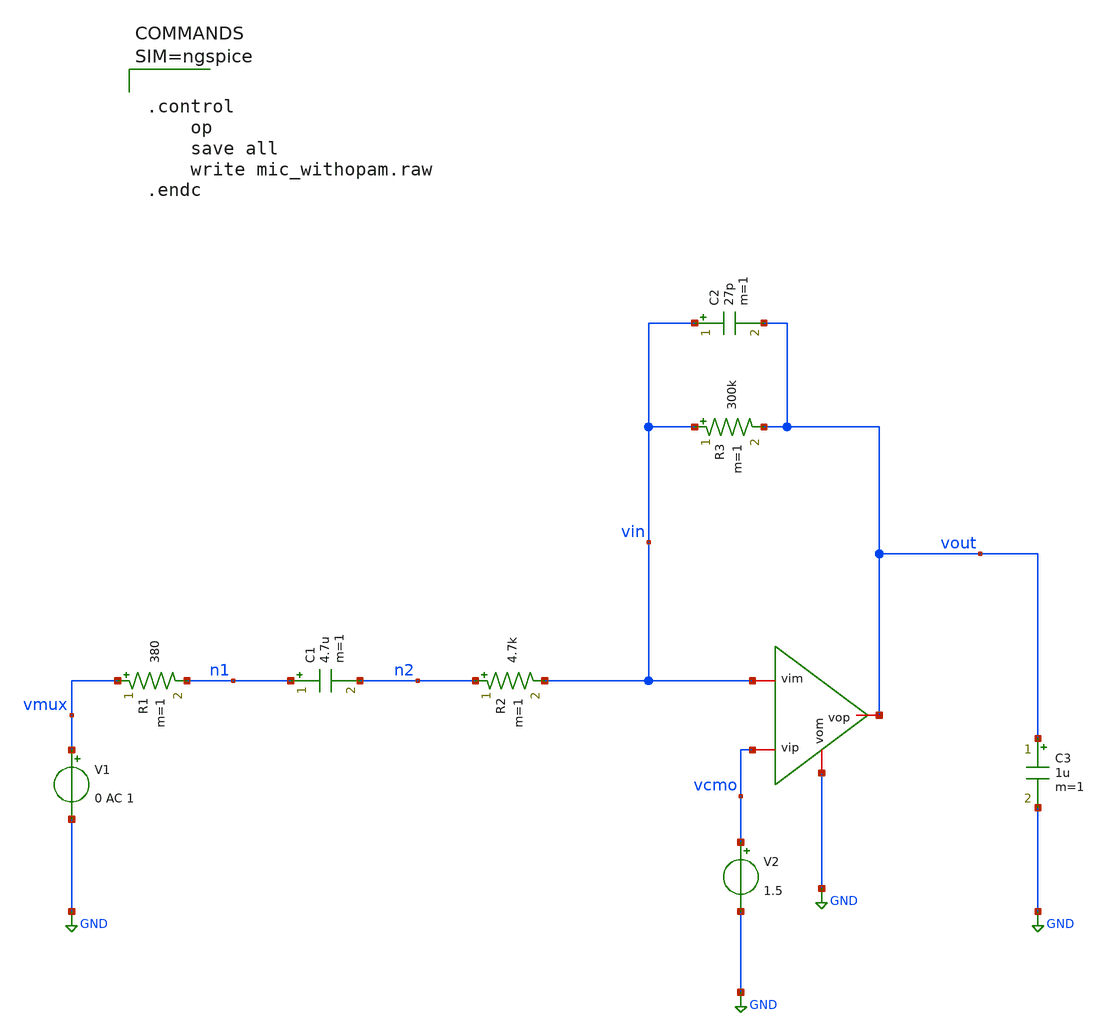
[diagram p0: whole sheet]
** sch_path: xschem/mic_withopam.sch
**.subckt mic_withopam
R1 vmux n1 380 m=1
C1 n1 n2 4.7u m=1
V1 vmux GND 0 AC 1
R2 n2 vin 4.7k m=1
V2 vcmo GND 1.5
R3 vin vout 300k m=1
C2 vin vout 27p m=1
C3 vout GND 1u m=1
x1 vout vcmo vin GND opam_mic1
**** begin user architecture code



.control
	op
	save all
	write mic_withopam.raw
.endc



**** end user architecture code
**.ends

* expanding   symbol:  /home/shubham/analoginternship/xschem-proj-1/xschem/opam_mic1.sym # of pins=4
** sym_path: xschem/opam_mic1.sym
** sch_path: xschem/opam_mic1.sch
.subckt opam_mic1 vop vip vim vom
*.iopin vip
*.iopin vim
*.iopin vop
*.iopin vom
E1 vop vom vip vim 1000
.ends

.GLOBAL GND
.end
